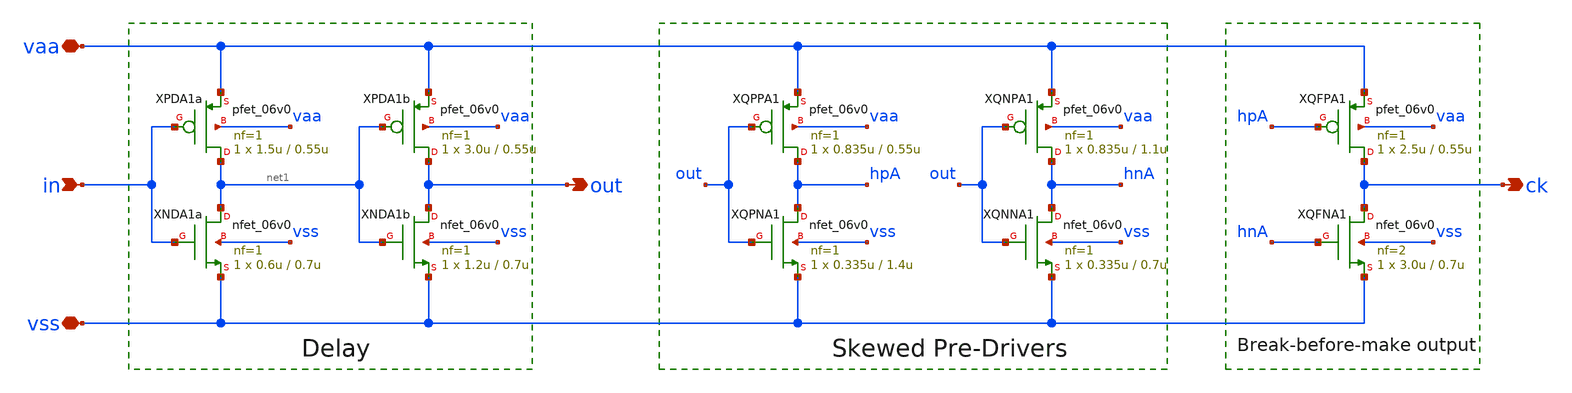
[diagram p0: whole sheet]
** sch_path: xschem/drv1_ph.sch
**.subckt drv1_ph vaa vss in out ck
*.iopin vaa
*.iopin vss
*.ipin in
*.opin out
*.opin ck
XPDA1a net1 in vaa vaa pfet_06v0 L=0.55u W=1.5u nf=1 ad='int((nf+1)/2) * W/nf * 0.18u' as='int((nf+2)/2) * W/nf * 0.18u'
+ pd='2*int((nf+1)/2) * (W/nf + 0.18u)' ps='2*int((nf+2)/2) * (W/nf + 0.18u)' nrd='0.18u / W' nrs='0.18u / W'
+ sa=0 sb=0 sd=0 m=1
XNDA1a net1 in vss vss nfet_06v0 L=0.7u W=0.6u nf=1 ad='int((nf+1)/2) * W/nf * 0.18u' as='int((nf+2)/2) * W/nf * 0.18u'
+ pd='2*int((nf+1)/2) * (W/nf + 0.18u)' ps='2*int((nf+2)/2) * (W/nf + 0.18u)' nrd='0.18u / W' nrs='0.18u / W'
+ sa=0 sb=0 sd=0 m=1 par=1
XPDA1b out net1 vaa vaa pfet_06v0 L=0.55u W=3.0u nf=1 ad='int((nf+1)/2) * W/nf * 0.18u' as='int((nf+2)/2) * W/nf * 0.18u'
+ pd='2*int((nf+1)/2) * (W/nf + 0.18u)' ps='2*int((nf+2)/2) * (W/nf + 0.18u)' nrd='0.18u / W' nrs='0.18u / W'
+ sa=0 sb=0 sd=0 m=1
XNDA1b out net1 vss vss nfet_06v0 L=0.7u W=1.2u nf=1 ad='int((nf+1)/2) * W/nf * 0.18u' as='int((nf+2)/2) * W/nf * 0.18u'
+ pd='2*int((nf+1)/2) * (W/nf + 0.18u)' ps='2*int((nf+2)/2) * (W/nf + 0.18u)' nrd='0.18u / W' nrs='0.18u / W'
+ sa=0 sb=0 sd=0 m=1 par=1
XQPPA1 hpA out vaa vaa pfet_06v0 L=0.55u W=0.835u nf=1 ad='int((nf+1)/2) * W/nf * 0.18u' as='int((nf+2)/2) * W/nf * 0.18u'
+ pd='2*int((nf+1)/2) * (W/nf + 0.18u)' ps='2*int((nf+2)/2) * (W/nf + 0.18u)' nrd='0.18u / W' nrs='0.18u / W'
+ sa=0 sb=0 sd=0 m=1
XQPNA1 hpA out vss vss nfet_06v0 L=1.4u W=0.335u nf=1 ad='int((nf+1)/2) * W/nf * 0.18u' as='int((nf+2)/2) * W/nf * 0.18u'
+ pd='2*int((nf+1)/2) * (W/nf + 0.18u)' ps='2*int((nf+2)/2) * (W/nf + 0.18u)' nrd='0.18u / W' nrs='0.18u / W'
+ sa=0 sb=0 sd=0 m=1 par=1
XQNPA1 hnA out vaa vaa pfet_06v0 L=1.1u W=0.835u nf=1 ad='int((nf+1)/2) * W/nf * 0.18u' as='int((nf+2)/2) * W/nf * 0.18u'
+ pd='2*int((nf+1)/2) * (W/nf + 0.18u)' ps='2*int((nf+2)/2) * (W/nf + 0.18u)' nrd='0.18u / W' nrs='0.18u / W'
+ sa=0 sb=0 sd=0 m=1
XQNNA1 hnA out vss vss nfet_06v0 L=0.7u W=0.335u nf=1 ad='int((nf+1)/2) * W/nf * 0.18u' as='int((nf+2)/2) * W/nf * 0.18u'
+ pd='2*int((nf+1)/2) * (W/nf + 0.18u)' ps='2*int((nf+2)/2) * (W/nf + 0.18u)' nrd='0.18u / W' nrs='0.18u / W'
+ sa=0 sb=0 sd=0 m=1 par=1
XQFPA1 ck hpA vaa vaa pfet_06v0 L=0.55u W=2.5u nf=1 ad='int((nf+1)/2) * W/nf * 0.18u' as='int((nf+2)/2) * W/nf * 0.18u'
+ pd='2*int((nf+1)/2) * (W/nf + 0.18u)' ps='2*int((nf+2)/2) * (W/nf + 0.18u)' nrd='0.18u / W' nrs='0.18u / W'
+ sa=0 sb=0 sd=0 m=1
XQFNA1 ck hnA vss vss nfet_06v0 L=0.7u W=3.0u nf=2 ad='int((nf+1)/2) * W/nf * 0.18u' as='int((nf+2)/2) * W/nf * 0.18u'
+ pd='2*int((nf+1)/2) * (W/nf + 0.18u)' ps='2*int((nf+2)/2) * (W/nf + 0.18u)' nrd='0.18u / W' nrs='0.18u / W'
+ sa=0 sb=0 sd=0 m=1 par=1
**.ends
.end
